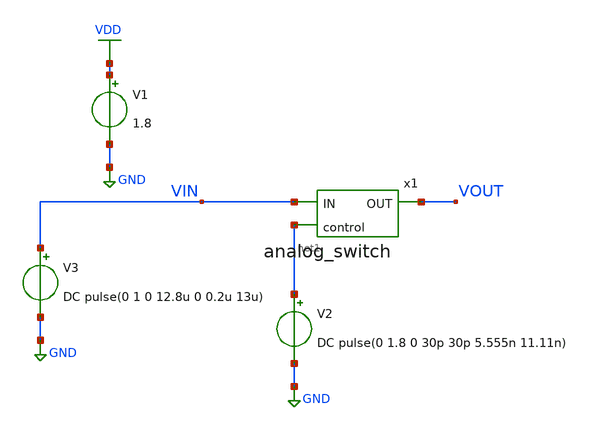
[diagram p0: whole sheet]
** sch_path: tb_switch.sch
* Copyright 2021 Stefan Frederik Schippers
* Licensed under the Apache License, Version 2.0 (the "License");
* you may not use this file except in compliance with the License.
* You may obtain a copy of the License at
* https://www.apache.org/licenses/LICENSE-2.0
* Unless required by applicable law or agreed to in writing, software
* distributed under the License is distributed on an "AS IS" BASIS,
* WITHOUT WARRANTIES OR CONDITIONS OF ANY KIND, either express or implied.
* See the License for the specific language governing permissions and
* limitations under the License.
**.subckt tb_switch
V2 net1 GND DC pulse(0 1.8 0 30p 30p 5.555n 11.11n)
V3 VIN GND DC pulse(0 1 0 12.8u 0 0.2u 13u)
V1 VDD GND 1.8
x1 net1 VOUT VIN analog_switch
**** begin user architecture code
 .lib $::SKYWATER_MODELS/sky130.lib.spice tt
.include $::SKYWATER_STDCELLS/sky130_fd_sc_hd.spice



.options acct list
.temp 25
.control
tran 30p 80n
write tb_saradc.raw
plot VIN VOUT
.endc


**** end user architecture code
**.ends
.GLOBAL GND
.GLOBAL VDD
.end
